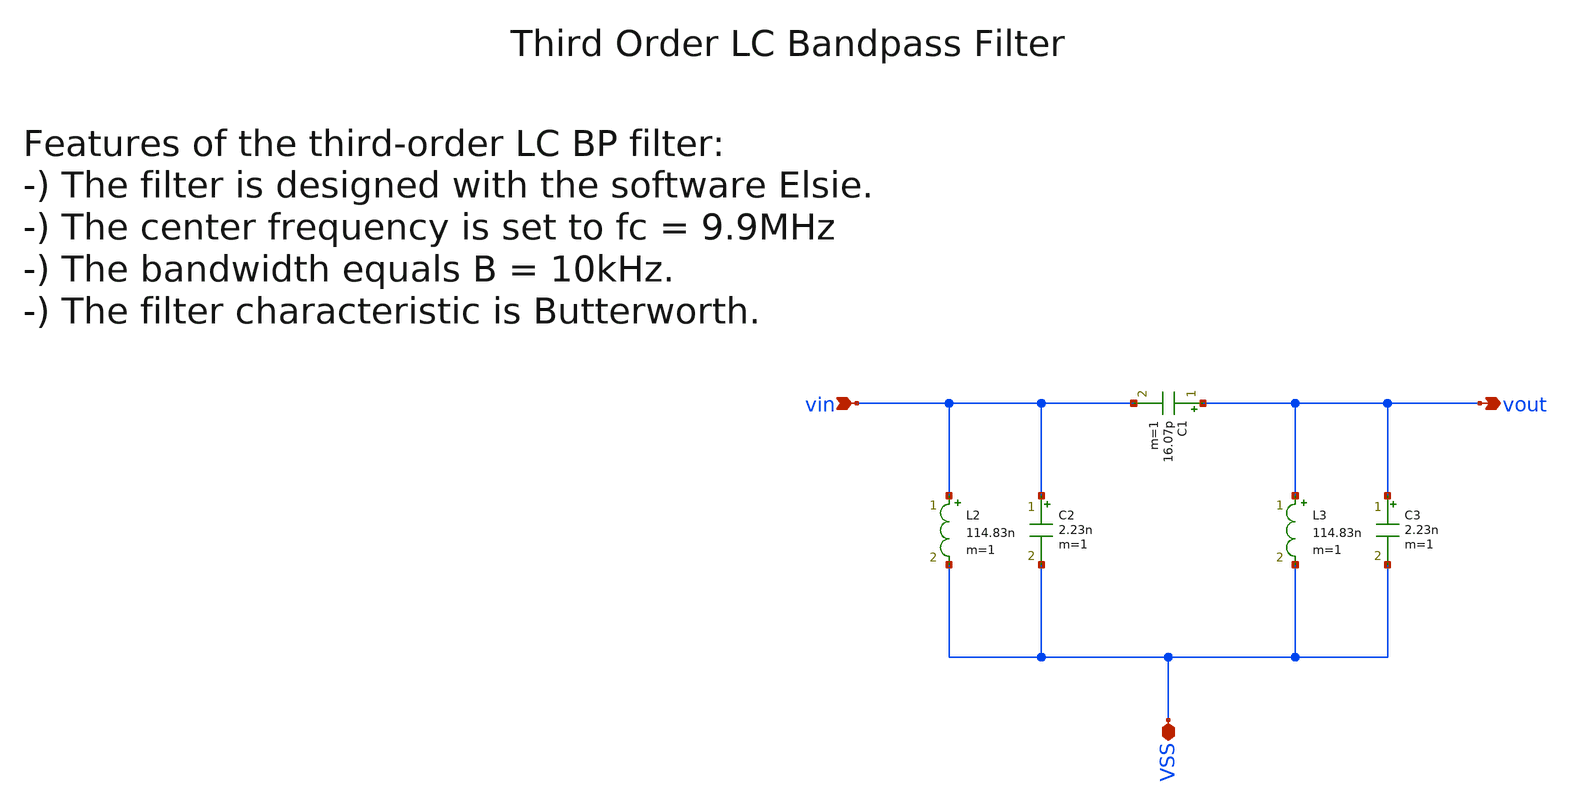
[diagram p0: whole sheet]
** sch_path: sky130/xschem/lc_bp_filter.sch
**.subckt lc_bp_filter vin vout VSS
*.ipin vin
*.opin vout
*.iopin VSS
C2 vin VSS 2.23n m=1
L2 vin VSS 114.83n m=1
C1 vout vin 16.07p m=1
C3 vout VSS 2.23n m=1
L3 vout VSS 114.83n m=1
**.ends
.end
